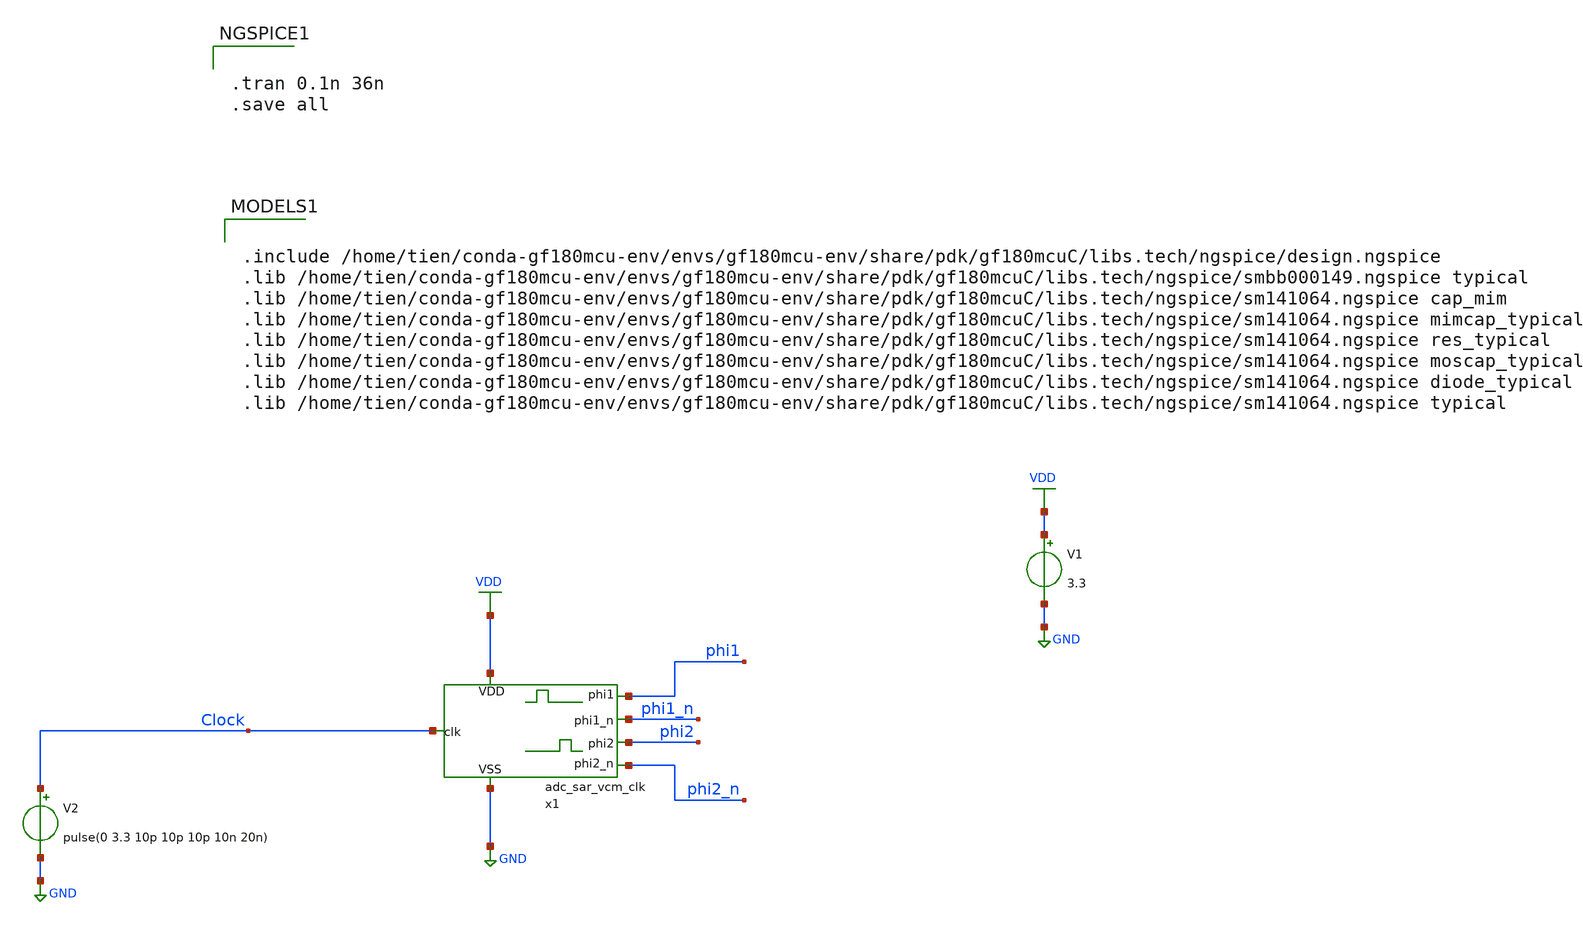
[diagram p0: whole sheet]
** sch_path: adc_sar_vcm_clk_tb.sch
**.subckt adc_sar_vcm_clk_tb
x1 VDD GND phi1_n phi1 phi2 phi2_n Clock adc_sar_vcm_clk
V1 VDD GND 3.3
V2 Clock GND pulse(0 3.3 10p 10p 10p 10n 20n)
**** begin user architecture code


.tran 0.1n 36n
.save all



.include /home/tien/conda-gf180mcu-env/envs/gf180mcu-env/share/pdk/gf180mcuC/libs.tech/ngspice/design.ngspice
.lib /home/tien/conda-gf180mcu-env/envs/gf180mcu-env/share/pdk/gf180mcuC/libs.tech/ngspice/smbb000149.ngspice typical
.lib /home/tien/conda-gf180mcu-env/envs/gf180mcu-env/share/pdk/gf180mcuC/libs.tech/ngspice/sm141064.ngspice cap_mim
.lib /home/tien/conda-gf180mcu-env/envs/gf180mcu-env/share/pdk/gf180mcuC/libs.tech/ngspice/sm141064.ngspice mimcap_typical
.lib /home/tien/conda-gf180mcu-env/envs/gf180mcu-env/share/pdk/gf180mcuC/libs.tech/ngspice/sm141064.ngspice res_typical
.lib /home/tien/conda-gf180mcu-env/envs/gf180mcu-env/share/pdk/gf180mcuC/libs.tech/ngspice/sm141064.ngspice moscap_typical
.lib /home/tien/conda-gf180mcu-env/envs/gf180mcu-env/share/pdk/gf180mcuC/libs.tech/ngspice/sm141064.ngspice diode_typical
.lib /home/tien/conda-gf180mcu-env/envs/gf180mcu-env/share/pdk/gf180mcuC/libs.tech/ngspice/sm141064.ngspice typical

**** end user architecture code
**.ends

* expanding   symbol:  adc_sar_vcm_clk.sym # of pins=7
** sym_path: adc_sar_vcm_clk.sym
** sch_path: adc_sar_vcm_clk.sch
.subckt adc_sar_vcm_clk VDD VSS phi1_n phi1 phi2 phi2_n clk
*.iopin VSS
*.iopin VDD
*.ipin clk
*.opin phi1
*.opin phi1_n
*.opin phi2
*.opin phi2_n
x1 VDD clk net17 net2 nand_gate
x2 VDD net16 net1 net3 nand_gate
x3 VDD VSS clk net1 adc_sar_inverter
x4 VDD VSS net2 net5 adc_sar_comp_buffer
x5 VDD VSS net3 net6 adc_sar_comp_buffer
XC1 net4 VSS cap_mim_1f0fF c_width=10e-6 c_length=50e-6 m=1
XR1 net5 net4 rm1 r_width=0.6e-6 r_length=17.4e-6 m=1
XC2 net7 VSS cap_mim_1f0fF c_width=10e-6 c_length=50e-6 m=1
XR2 net6 net7 rm1 r_width=0.6e-6 r_length=17.4e-6 m=1
x6 VDD VSS net4 net11 adc_sar_comp_buffer
x7 VDD VSS net7 net10 adc_sar_comp_buffer
XC3 net8 VSS cap_mim_1f0fF c_width=10e-6 c_length=50e-6 m=1
XR3 net11 net8 rm1 r_width=0.6e-6 r_length=17.4e-6 m=1
XC4 net9 VSS cap_mim_1f0fF c_width=10e-6 c_length=50e-6 m=1
XR4 net10 net9 rm1 r_width=0.6e-6 r_length=17.4e-6 m=1
x8 VDD VSS net8 net12 adc_sar_comp_buffer
x9 VDD VSS net9 net13 adc_sar_comp_buffer
x10 VDD VSS net12 net14 adc_sar_inverter
x11 VDD VSS net13 net15 adc_sar_inverter
x12 VDD VSS net14 net16 adc_sar_inverter
x13 VDD VSS net15 net17 adc_sar_inverter
x14 VDD VSS net16 phi1_n adc_sar_comp_buffer
x15 VDD VSS net17 phi2 adc_sar_comp_buffer
x16 VDD VSS net14 phi1 adc_sar_comp_buffer
x17 VDD VSS net15 phi2_n adc_sar_comp_buffer
.ends


* expanding   symbol:  nand_gate.sym # of pins=4
** sym_path: nand_gate.sym
** sch_path: nand_gate.sch
.subckt nand_gate VP A B Y
*.ipin A
*.ipin B
*.opin Y
*.iopin VP
XM1 Y B net1 GND nfet_03v3 L=0.28u W=0.22u nf=1 ad='int((nf+1)/2) * W/nf * 0.18u' as='int((nf+2)/2) * W/nf * 0.18u'
+ pd='2*int((nf+1)/2) * (W/nf + 0.18u)' ps='2*int((nf+2)/2) * (W/nf + 0.18u)' nrd='0.18u / W' nrs='0.18u / W'
+ sa=0 sb=0 sd=0 m=1
XM2 Y A VP VP pfet_03v3 L=0.28u W=1u nf=1 ad='int((nf+1)/2) * W/nf * 0.18u' as='int((nf+2)/2) * W/nf * 0.18u'
+ pd='2*int((nf+1)/2) * (W/nf + 0.18u)' ps='2*int((nf+2)/2) * (W/nf + 0.18u)' nrd='0.18u / W' nrs='0.18u / W'
+ sa=0 sb=0 sd=0 m=1
XM4 net1 A GND GND nfet_03v3 L=0.28u W=0.22u nf=1 ad='int((nf+1)/2) * W/nf * 0.18u' as='int((nf+2)/2) * W/nf * 0.18u'
+ pd='2*int((nf+1)/2) * (W/nf + 0.18u)' ps='2*int((nf+2)/2) * (W/nf + 0.18u)' nrd='0.18u / W' nrs='0.18u / W'
+ sa=0 sb=0 sd=0 m=1
XM3 Y B VP VP pfet_03v3 L=0.28u W=1u nf=1 ad='int((nf+1)/2) * W/nf * 0.18u' as='int((nf+2)/2) * W/nf * 0.18u'
+ pd='2*int((nf+1)/2) * (W/nf + 0.18u)' ps='2*int((nf+2)/2) * (W/nf + 0.18u)' nrd='0.18u / W' nrs='0.18u / W'
+ sa=0 sb=0 sd=0 m=1
.ends


* expanding   symbol:  adc_sar_inverter.sym # of pins=4
** sym_path: adc_sar_inverter.sym
** sch_path: adc_sar_inverter.sch
.subckt adc_sar_inverter VDD VSS in out
*.iopin VDD
*.iopin VSS
*.ipin in
*.opin out
XM1 out in VSS VSS nfet_03v3 L=0.28u W=0.42u nf=1 ad='int((nf+1)/2) * W/nf * 0.18u' as='int((nf+2)/2) * W/nf * 0.18u'
+ pd='2*int((nf+1)/2) * (W/nf + 0.18u)' ps='2*int((nf+2)/2) * (W/nf + 0.18u)' nrd='0.18u / W' nrs='0.18u / W'
+ sa=0 sb=0 sd=0 m=1
XM2 out in VDD VDD pfet_03v3 L=0.28u W=0.84u nf=1 ad='int((nf+1)/2) * W/nf * 0.18u' as='int((nf+2)/2) * W/nf * 0.18u'
+ pd='2*int((nf+1)/2) * (W/nf + 0.18u)' ps='2*int((nf+2)/2) * (W/nf + 0.18u)' nrd='0.18u / W' nrs='0.18u / W'
+ sa=0 sb=0 sd=0 m=1
.ends


* expanding   symbol:  adc_sar_comp_buffer.sym # of pins=4
** sym_path: adc_sar_comp_buffer.sym
** sch_path: adc_sar_comp_buffer.sch
.subckt adc_sar_comp_buffer VDD VSS in out
*.iopin VDD
*.iopin VSS
*.ipin in
*.opin out
XM1 buf_mid in VSS VSS nfet_03v3 L=0.28u W=0.5u nf=1 ad='int((nf+1)/2) * W/nf * 0.18u' as='int((nf+2)/2) * W/nf * 0.18u'
+ pd='2*int((nf+1)/2) * (W/nf + 0.18u)' ps='2*int((nf+2)/2) * (W/nf + 0.18u)' nrd='0.18u / W' nrs='0.18u / W'
+ sa=0 sb=0 sd=0 m=1
XM2 out buf_mid VSS VSS nfet_03v3 L=0.28u W=1u nf=1 ad='int((nf+1)/2) * W/nf * 0.18u' as='int((nf+2)/2) * W/nf * 0.18u'
+ pd='2*int((nf+1)/2) * (W/nf + 0.18u)' ps='2*int((nf+2)/2) * (W/nf + 0.18u)' nrd='0.18u / W' nrs='0.18u / W'
+ sa=0 sb=0 sd=0 m=1
XM3 buf_mid in VDD VDD pfet_03v3 L=0.28u W=1u nf=1 ad='int((nf+1)/2) * W/nf * 0.18u' as='int((nf+2)/2) * W/nf * 0.18u'
+ pd='2*int((nf+1)/2) * (W/nf + 0.18u)' ps='2*int((nf+2)/2) * (W/nf + 0.18u)' nrd='0.18u / W' nrs='0.18u / W'
+ sa=0 sb=0 sd=0 m=1
XM4 out buf_mid VDD VDD pfet_03v3 L=0.28u W=2u nf=1 ad='int((nf+1)/2) * W/nf * 0.18u' as='int((nf+2)/2) * W/nf * 0.18u'
+ pd='2*int((nf+1)/2) * (W/nf + 0.18u)' ps='2*int((nf+2)/2) * (W/nf + 0.18u)' nrd='0.18u / W' nrs='0.18u / W'
+ sa=0 sb=0 sd=0 m=1
.ends

.GLOBAL GND
.GLOBAL VDD
.end
